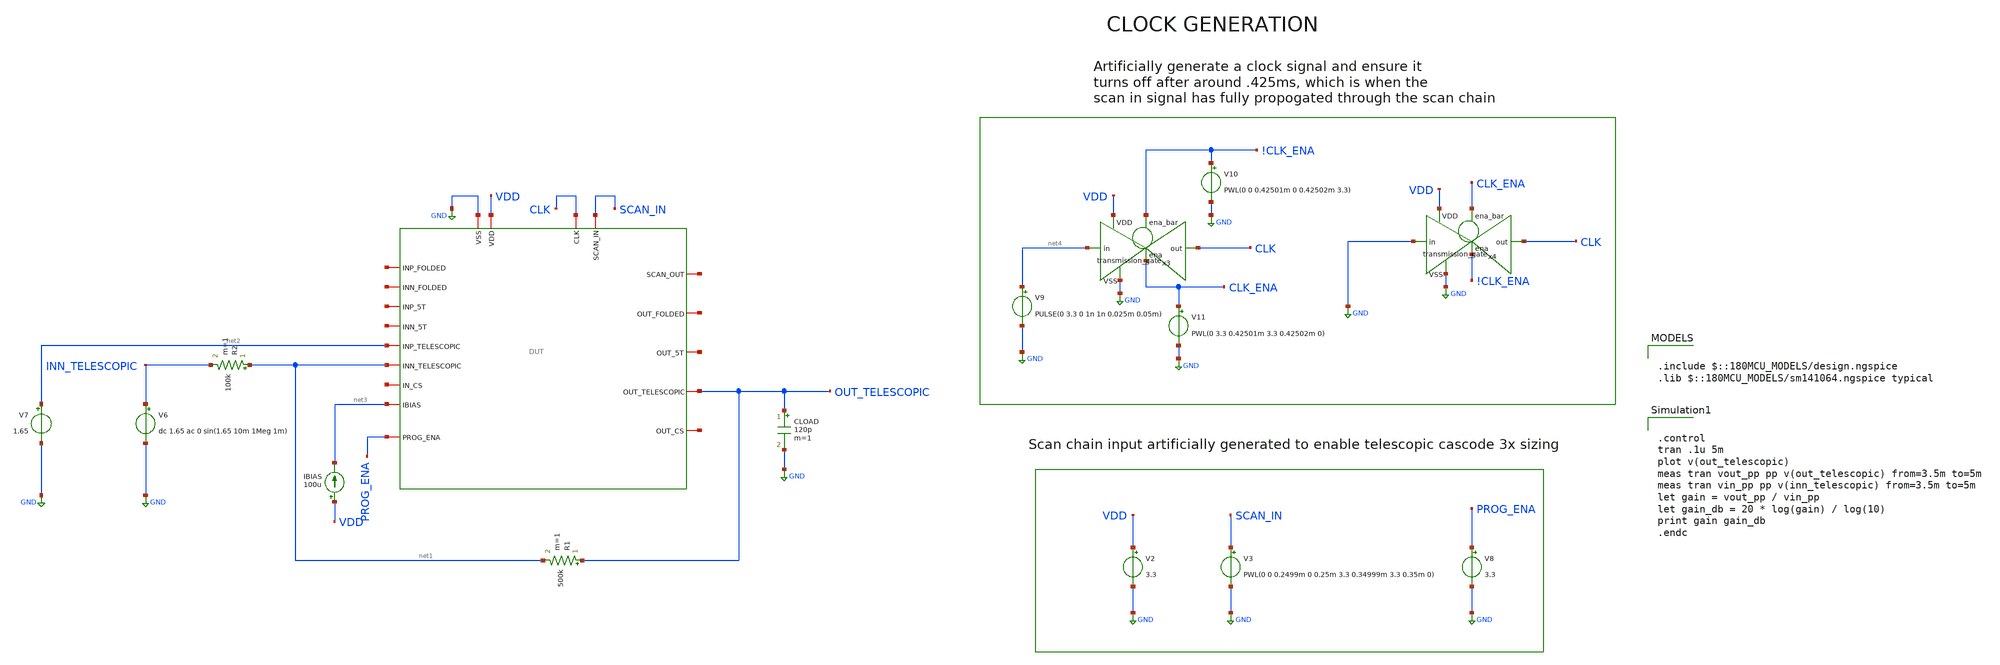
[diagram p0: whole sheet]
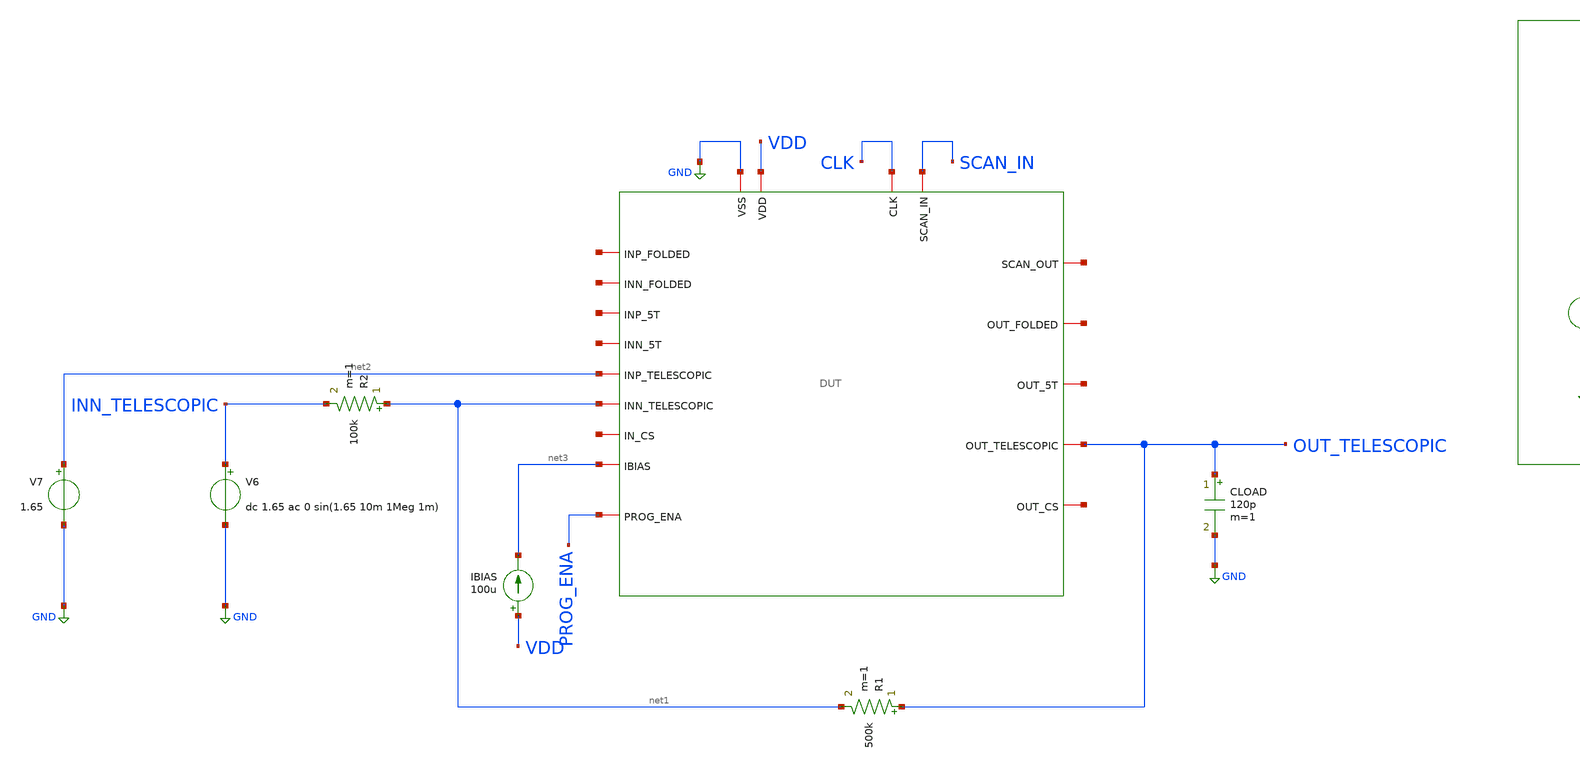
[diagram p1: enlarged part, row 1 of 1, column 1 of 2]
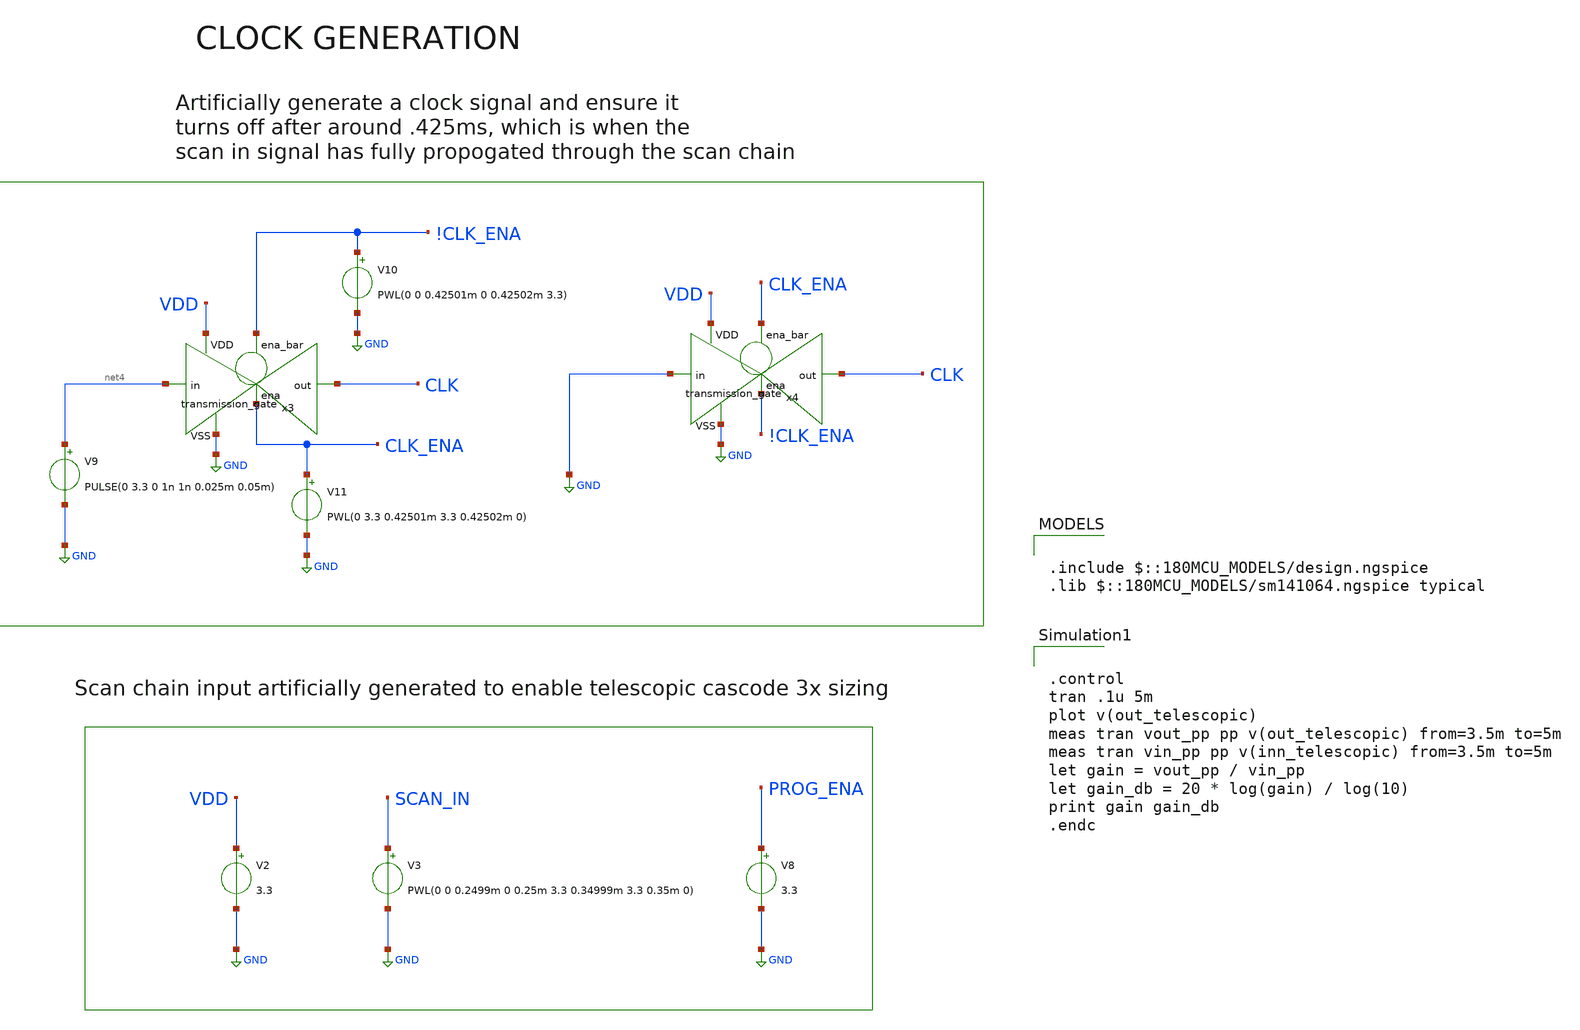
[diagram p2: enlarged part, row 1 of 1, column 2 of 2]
** sch_path: designs/libs/verification/ota_telescopic/4x/bw.sch
**.subckt bw
x1 CLK net5 SCAN_IN GND VDD net6 net7 net8 net3 net9 net10 net11 net2 OUT_TELESCOPIC net12 net13
+ net1 PROG_ENA DUT
CLOAD OUT_TELESCOPIC GND 120p m=1
R1 OUT_TELESCOPIC net1 500k m=1
R2 net1 INN_TELESCOPIC 100k m=1
V6 INN_TELESCOPIC GND dc 1.65 ac 0 sin(1.65 10m 1Meg 1m)
V7 net2 GND 1.65
IBIAS VDD net3 100u
V2 VDD GND 3.3
V8 PROG_ENA GND 3.3
V9 net4 GND PULSE(0 3.3 0 1n 1n 0.025m 0.05m)
x3 !CLK_ENA VDD CLK net4 GND CLK_ENA transmission_gate
V10 !CLK_ENA GND PWL(0 0 0.42501m 0 0.42502m 3.3)
V11 CLK_ENA GND PWL(0 3.3 0.42501m 3.3 0.42502m 0)
x4 CLK_ENA VDD CLK GND GND !CLK_ENA transmission_gate
V3 SCAN_IN GND PWL(0 0 0.2499m 0 0.25m 3.3 0.34999m 3.3 0.35m 0)
**** begin user architecture code

.include $::180MCU_MODELS/design.ngspice
.lib $::180MCU_MODELS/sm141064.ngspice typical



.control
tran .1u 5m
plot v(out_telescopic)
meas tran vout_pp pp v(out_telescopic) from=3.5m to=5m
meas tran vin_pp pp v(inn_telescopic) from=3.5m to=5m
let gain = vout_pp / vin_pp
let gain_db = 20 * log(gain) / log(10)
print gain gain_db
.endc


**** end user architecture code
**.ends
.GLOBAL GND
.end
